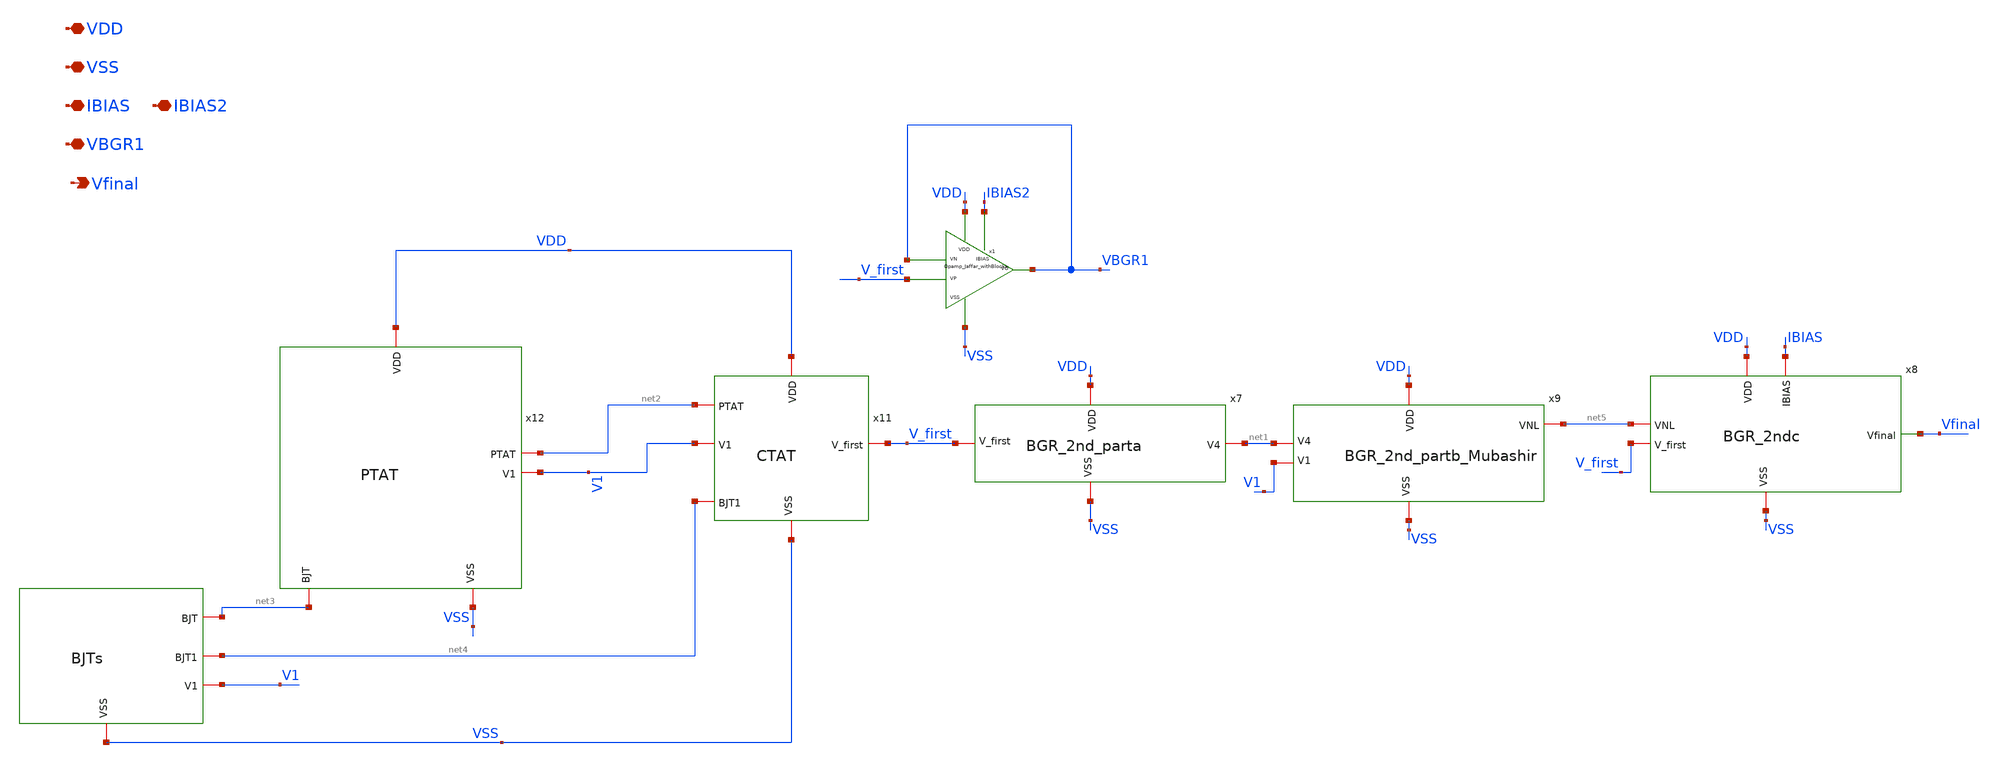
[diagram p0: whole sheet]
** sch_path: xschem/xschem_BGR_Top/BGR_Toplevel.sch
**.subckt BGR_Toplevel Vfinal VDD VSS VBGR1 IBIAS IBIAS2
*.opin Vfinal
*.iopin VDD
*.iopin VSS
*.iopin VBGR1
*.iopin IBIAS
*.iopin IBIAS2
x7 VDD VSS V_first net1 BGR_2nd_parta
x8 VDD VSS net5 V_first IBIAS Vfinal BGR_2ndc
x9 VDD VSS V1 net1 net5 BGR_2nd_partb_Mubashir
x10 net3 VSS net4 V1 BJTs
x11 VDD net2 V1 V_first VSS net4 CTAT
x12 VDD net2 V1 net3 VSS PTAT
x1 VDD VSS V_first VBGR1 VBGR1 IBIAS2 Opamp_Jaffar_withBlocks
**.ends
.end
